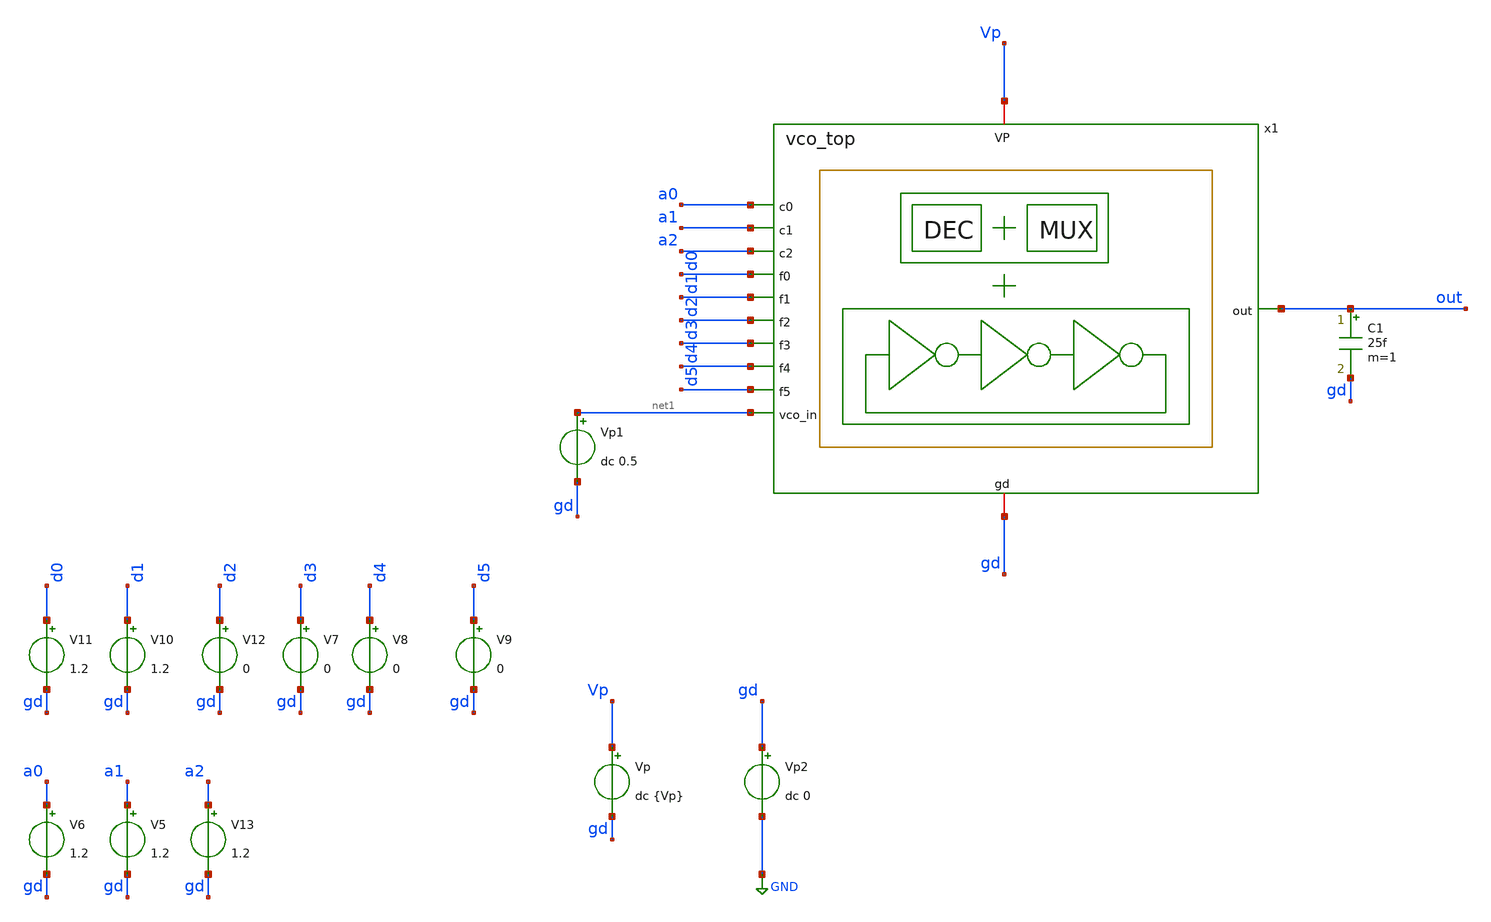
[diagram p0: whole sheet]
** sch_path: PLL0663-main/testbenches/tran/xschem/vco/vco_top_tb.sch
**.subckt vco_top_tb
x1 out gd Vp a0 a1 a2 d0 d1 d2 d3 d4 d5 net1 vco_top
V8 d4 gd 0
V9 d5 gd 0
V11 d0 gd 1.2
V10 d1 gd 1.2
V12 d2 gd 0
V7 d3 gd 0
V5 a1 gd 1.2
V6 a0 gd 1.2
V13 a2 gd 1.2
Vp Vp gd dc {Vp}
Vp2 gd GND dc 0
Vp1 net1 gd dc 0.5
C1 out gd 25f m=1
**** begin user architecture code


.temp=25
.param T = 31.25u
.option klu method=gear reltol=1e-3 gmin=1e-12 abstol=1e-12 rshunt=1e12
.options cshunt=2.5f
.param Vp=1.2
.param Vph=3.3
.control

* Operating Point Analysis



write vco_top_tb.raw
set appendwrite
save all
tran 0.1n 100u


write PLL_top_tb.raw
.endc


**** end user architecture code
**.ends
.GLOBAL GND
.end
